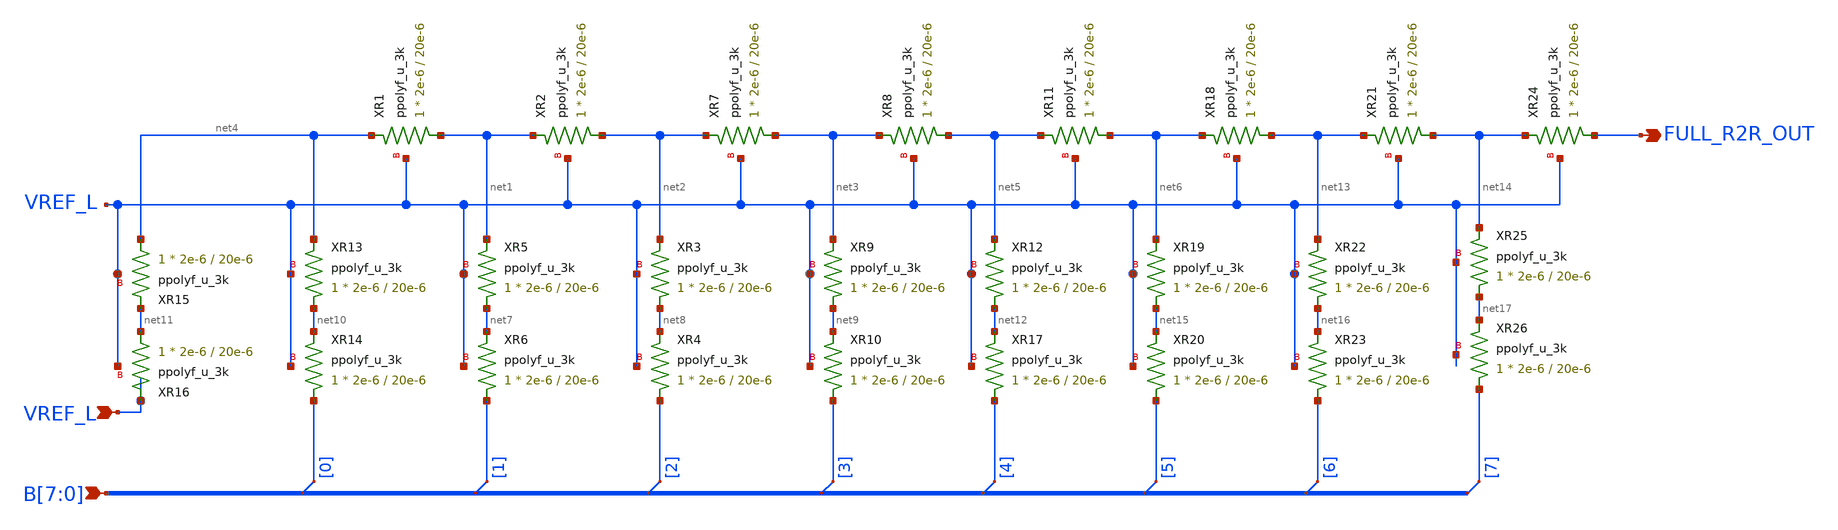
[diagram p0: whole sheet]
** sch_path: xschem/8_bit_r2r.sch
**.subckt 8_bit_r2r FULL_R2R_OUT VREF_L B[7],B[6],B[5],B[4],B[3],B[2],B[1],B[0]
*.opin FULL_R2R_OUT
*.ipin VREF_L
*.ipin B[7],B[6],B[5],B[4],B[3],B[2],B[1],B[0]
XR1 net1 net4 VREF_L ppolyf_u_3k r_width=2e-6 r_length=20e-6 m=1
XR2 net2 net1 VREF_L ppolyf_u_3k r_width=2e-6 r_length=20e-6 m=1
XR5 net7 net1 VREF_L ppolyf_u_3k r_width=2e-6 r_length=20e-6 m=1
XR6 B[1] net7 VREF_L ppolyf_u_3k r_width=2e-6 r_length=20e-6 m=1
XR3 net8 net2 VREF_L ppolyf_u_3k r_width=2e-6 r_length=20e-6 m=1
XR4 B[2] net8 VREF_L ppolyf_u_3k r_width=2e-6 r_length=20e-6 m=1
XR7 net3 net2 VREF_L ppolyf_u_3k r_width=2e-6 r_length=20e-6 m=1
XR8 net5 net3 VREF_L ppolyf_u_3k r_width=2e-6 r_length=20e-6 m=1
XR9 net9 net3 VREF_L ppolyf_u_3k r_width=2e-6 r_length=20e-6 m=1
XR10 B[3] net9 VREF_L ppolyf_u_3k r_width=2e-6 r_length=20e-6 m=1
XR13 net10 net4 VREF_L ppolyf_u_3k r_width=2e-6 r_length=20e-6 m=1
XR14 B[0] net10 VREF_L ppolyf_u_3k r_width=2e-6 r_length=20e-6 m=1
XR15 net4 net11 VREF_L ppolyf_u_3k r_width=2e-6 r_length=20e-6 m=1
XR16 net11 VREF_L VREF_L ppolyf_u_3k r_width=2e-6 r_length=20e-6 m=1
XR11 net6 net5 VREF_L ppolyf_u_3k r_width=2e-6 r_length=20e-6 m=1
XR12 net12 net5 VREF_L ppolyf_u_3k r_width=2e-6 r_length=20e-6 m=1
XR17 B[4] net12 VREF_L ppolyf_u_3k r_width=2e-6 r_length=20e-6 m=1
* tap: B[7:0] --> B[0]
* tap: B[7:0] --> B[1]
* tap: B[7:0] --> B[2]
* tap: B[7:0] --> B[3]
* tap: B[7:0] --> B[4]
XR18 net13 net6 VREF_L ppolyf_u_3k r_width=2e-6 r_length=20e-6 m=1
XR19 net15 net6 VREF_L ppolyf_u_3k r_width=2e-6 r_length=20e-6 m=1
XR20 B[5] net15 VREF_L ppolyf_u_3k r_width=2e-6 r_length=20e-6 m=1
XR21 net14 net13 VREF_L ppolyf_u_3k r_width=2e-6 r_length=20e-6 m=1
XR22 net16 net13 VREF_L ppolyf_u_3k r_width=2e-6 r_length=20e-6 m=1
XR23 B[6] net16 VREF_L ppolyf_u_3k r_width=2e-6 r_length=20e-6 m=1
* tap: B[7:0] --> B[5]
* tap: B[7:0] --> B[6]
XR24 FULL_R2R_OUT net14 VREF_L ppolyf_u_3k r_width=2e-6 r_length=20e-6 m=1
* tap: B[7:0] --> B[7]
XR25 net17 net14 VREF_L ppolyf_u_3k r_width=2e-6 r_length=20e-6 m=1
XR26 B[7] net17 VREF_L ppolyf_u_3k r_width=2e-6 r_length=20e-6 m=1
**.ends
.end
